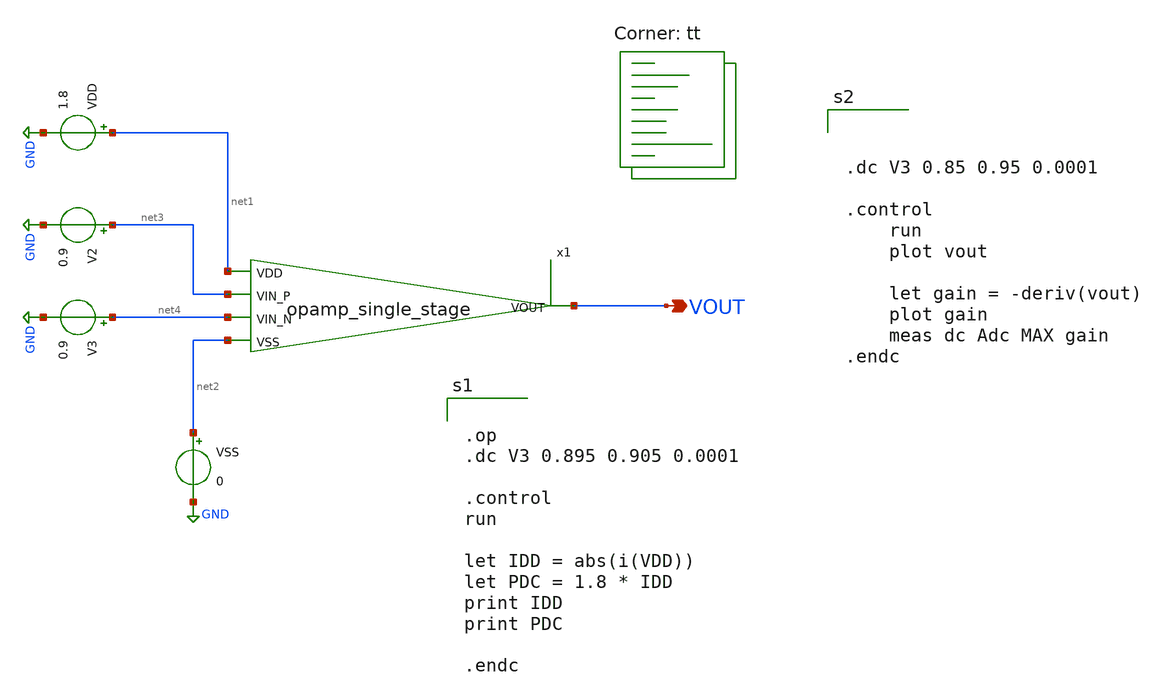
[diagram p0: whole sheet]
** sch_path: analog/schematics/testbenches/tb_dc_analysis.sch
**.subckt tb_dc_analysis VOUT
*.opin VOUT
VDD net1 GND 1.8
VSS net2 GND 0
V2 net3 GND 0.9
V3 net4 GND 0.9
x1 net1 VOUT net3 net4 net2 opamp_single_stage
**** begin user architecture code
.lib $::SKYWATER_MODELS/sky130.lib.spice tt



.dc V3 0.85 0.95 0.0001

.control
    run
    plot vout

    let gain = -deriv(vout)
    plot gain
    meas dc Adc MAX gain
.endc






.op
.dc V3 0.895 0.905 0.0001

.control
run

let IDD = abs(i(VDD))
let PDC = 1.8 * IDD
print IDD
print PDC

.endc



**** end user architecture code
**.ends

* expanding   symbol:  opamp_single_stage.sym # of pins=5
** sym_path: analog/schematics/opamp_single_stage.sym
** sch_path: analog/schematics/opamp_single_stage.sch
.subckt opamp_single_stage VDD VOUT VIN_P VIN_N VSS
*.ipin VDD
*.ipin VIN_P
*.ipin VSS
*.opin VOUT
*.ipin VIN_N
XM4 net2 net1 VDD VDD sky130_fd_pr__pfet_01v8 L=0.5 W=8 nf=1 ad='int((nf+1)/2) * W/nf * 0.29' as='int((nf+2)/2) * W/nf * 0.29'
+ pd='2*int((nf+1)/2) * (W/nf + 0.29)' ps='2*int((nf+2)/2) * (W/nf + 0.29)' nrd='0.29 / W' nrs='0.29 / W'
+ sa=0 sb=0 sd=0 mult=1 m=1
XM3 net1 net1 VDD VDD sky130_fd_pr__pfet_01v8 L=0.5 W=8 nf=1 ad='int((nf+1)/2) * W/nf * 0.29' as='int((nf+2)/2) * W/nf * 0.29'
+ pd='2*int((nf+1)/2) * (W/nf + 0.29)' ps='2*int((nf+2)/2) * (W/nf + 0.29)' nrd='0.29 / W' nrs='0.29 / W'
+ sa=0 sb=0 sd=0 mult=1 m=1
XM1 net1 VIN_N net3 GND sky130_fd_pr__nfet_01v8_lvt L=0.5 W=6 nf=1 ad='int((nf+1)/2) * W/nf * 0.29' as='int((nf+2)/2) * W/nf * 0.29'
+ pd='2*int((nf+1)/2) * (W/nf + 0.29)' ps='2*int((nf+2)/2) * (W/nf + 0.29)' nrd='0.29 / W' nrs='0.29 / W'
+ sa=0 sb=0 sd=0 mult=1 m=1
XM2 net2 VIN_P net3 GND sky130_fd_pr__nfet_01v8_lvt L=0.5 W=6 nf=1 ad='int((nf+1)/2) * W/nf * 0.29' as='int((nf+2)/2) * W/nf * 0.29'
+ pd='2*int((nf+1)/2) * (W/nf + 0.29)' ps='2*int((nf+2)/2) * (W/nf + 0.29)' nrd='0.29 / W' nrs='0.29 / W'
+ sa=0 sb=0 sd=0 mult=1 m=1
XM5 VOUT net2 VDD VDD sky130_fd_pr__pfet_01v8 L=0.5 W=20 nf=1 ad='int((nf+1)/2) * W/nf * 0.29' as='int((nf+2)/2) * W/nf * 0.29'
+ pd='2*int((nf+1)/2) * (W/nf + 0.29)' ps='2*int((nf+2)/2) * (W/nf + 0.29)' nrd='0.29 / W' nrs='0.29 / W'
+ sa=0 sb=0 sd=0 mult=1 m=1
XC1 net5 VOUT sky130_fd_pr__cap_mim_m3_1 W=25 L=20 MF=1 m=1
XM8 net4 net4 VSS VSS sky130_fd_pr__nfet_01v8_lvt L=1.0 W=2 nf=1 ad='int((nf+1)/2) * W/nf * 0.29' as='int((nf+2)/2) * W/nf * 0.29'
+ pd='2*int((nf+1)/2) * (W/nf + 0.29)' ps='2*int((nf+2)/2) * (W/nf + 0.29)' nrd='0.29 / W' nrs='0.29 / W'
+ sa=0 sb=0 sd=0 mult=1 m=1
XM7 net3 net4 VSS VSS sky130_fd_pr__nfet_01v8_lvt L=1.0 W=4 nf=1 ad='int((nf+1)/2) * W/nf * 0.29' as='int((nf+2)/2) * W/nf * 0.29'
+ pd='2*int((nf+1)/2) * (W/nf + 0.29)' ps='2*int((nf+2)/2) * (W/nf + 0.29)' nrd='0.29 / W' nrs='0.29 / W'
+ sa=0 sb=0 sd=0 mult=1 m=1
XM6 VOUT net4 VSS VSS sky130_fd_pr__nfet_01v8_lvt L=1.0 W=8 nf=1 ad='int((nf+1)/2) * W/nf * 0.29' as='int((nf+2)/2) * W/nf * 0.29'
+ pd='2*int((nf+1)/2) * (W/nf + 0.29)' ps='2*int((nf+2)/2) * (W/nf + 0.29)' nrd='0.29 / W' nrs='0.29 / W'
+ sa=0 sb=0 sd=0 mult=1 m=1
R1 net5 net2 7k m=1
XR2 net4 VDD VDD sky130_fd_pr__res_high_po W=0.35 L=14 mult=1 m=1
.ends

.GLOBAL GND
.end
